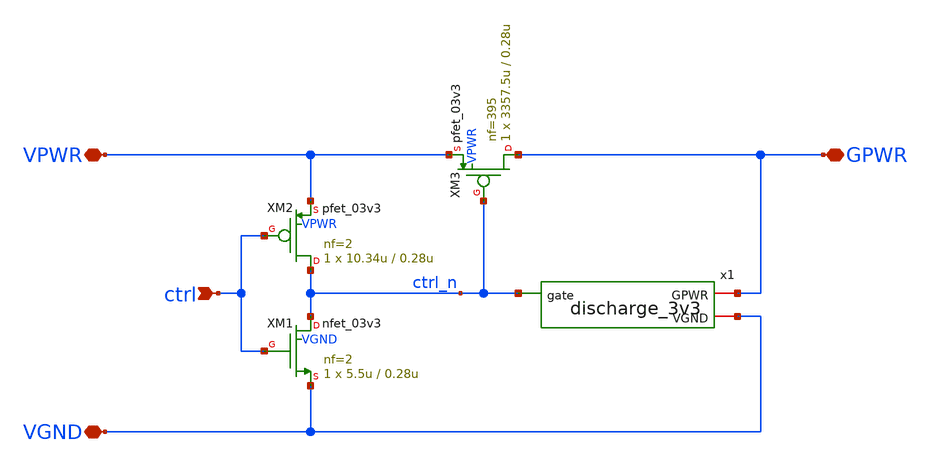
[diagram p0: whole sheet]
** sch_path: pg/gf180mcuD/tt_pg_3v3_hp_2/xschem/tt_pg_3v3_hp_2.sch
**.subckt tt_pg_3v3_hp_2 ctrl VPWR VGND GPWR
*.ipin ctrl
*.iopin VPWR
*.iopin VGND
*.iopin GPWR
x1 VGND GPWR ctrl_n discharge_3v3
XM1 ctrl_n ctrl VGND VGND nfet_03v3 L=0.28u W=5.5u nf=2 ad='int((nf+1)/2) * W/nf * 0.18u' as='int((nf+2)/2) * W/nf * 0.18u'
+ pd='2*int((nf+1)/2) * (W/nf + 0.18u)' ps='2*int((nf+2)/2) * (W/nf + 0.18u)' nrd='0.18u / W' nrs='0.18u / W'
+ sa=0 sb=0 sd=0 m=1 par=1
XM2 ctrl_n ctrl VPWR VPWR pfet_03v3 L=0.28u W=10.34u nf=2 ad='int((nf+1)/2) * W/nf * 0.18u' as='int((nf+2)/2) * W/nf * 0.18u'
+ pd='2*int((nf+1)/2) * (W/nf + 0.18u)' ps='2*int((nf+2)/2) * (W/nf + 0.18u)' nrd='0.18u / W' nrs='0.18u / W'
+ sa=0 sb=0 sd=0 m=1 par=1
XM3 GPWR ctrl_n VPWR VPWR pfet_03v3 L=0.28u W=3357.5u nf=395 ad='int((nf+1)/2) * W/nf * 0.18u' as='int((nf+2)/2) * W/nf * 0.18u'
+ pd='2*int((nf+1)/2) * (W/nf + 0.18u)' ps='2*int((nf+2)/2) * (W/nf + 0.18u)' nrd='0.18u / W' nrs='0.18u / W'
+ sa=0 sb=0 sd=0 m=1 par=1
**.ends

* expanding   symbol:  discharge_3v3.sym # of pins=3
** sym_path: pg/gf180mcuD/common/xschem/discharge_3v3.sym
** sch_path: pg/gf180mcuD/common/xschem/discharge_3v3.sch
.subckt discharge_3v3 VGND GPWR gate
*.iopin GPWR
*.iopin VGND
*.ipin gate
XM1 GPWR gate net3 VGND nfet_03v3 L=0.6u W=0.99u nf=1 ad='int((nf+1)/2) * W/nf * 0.18u' as='int((nf+2)/2) * W/nf * 0.18u'
+ pd='2*int((nf+1)/2) * (W/nf + 0.18u)' ps='2*int((nf+2)/2) * (W/nf + 0.18u)' nrd='0.18u / W' nrs='0.18u / W'
+ sa=0 sb=0 sd=0 m=1 par=1
XM2 net3 gate net2 VGND nfet_03v3 L=0.6u W=0.99u nf=1 ad='int((nf+1)/2) * W/nf * 0.18u' as='int((nf+2)/2) * W/nf * 0.18u'
+ pd='2*int((nf+1)/2) * (W/nf + 0.18u)' ps='2*int((nf+2)/2) * (W/nf + 0.18u)' nrd='0.18u / W' nrs='0.18u / W'
+ sa=0 sb=0 sd=0 m=1 par=1
XM3 net2 gate net1 VGND nfet_03v3 L=0.6u W=0.99u nf=1 ad='int((nf+1)/2) * W/nf * 0.18u' as='int((nf+2)/2) * W/nf * 0.18u'
+ pd='2*int((nf+1)/2) * (W/nf + 0.18u)' ps='2*int((nf+2)/2) * (W/nf + 0.18u)' nrd='0.18u / W' nrs='0.18u / W'
+ sa=0 sb=0 sd=0 m=1 par=1
XM4 net1 gate VGND VGND nfet_03v3 L=0.6u W=0.99u nf=1 ad='int((nf+1)/2) * W/nf * 0.18u' as='int((nf+2)/2) * W/nf * 0.18u'
+ pd='2*int((nf+1)/2) * (W/nf + 0.18u)' ps='2*int((nf+2)/2) * (W/nf + 0.18u)' nrd='0.18u / W' nrs='0.18u / W'
+ sa=0 sb=0 sd=0 m=1 par=1
XM5 GPWR gate net6 VGND nfet_03v3 L=0.6u W=0.99u nf=1 ad='int((nf+1)/2) * W/nf * 0.18u' as='int((nf+2)/2) * W/nf * 0.18u'
+ pd='2*int((nf+1)/2) * (W/nf + 0.18u)' ps='2*int((nf+2)/2) * (W/nf + 0.18u)' nrd='0.18u / W' nrs='0.18u / W'
+ sa=0 sb=0 sd=0 m=1 par=1
XM6 net6 gate net5 VGND nfet_03v3 L=0.6u W=0.99u nf=1 ad='int((nf+1)/2) * W/nf * 0.18u' as='int((nf+2)/2) * W/nf * 0.18u'
+ pd='2*int((nf+1)/2) * (W/nf + 0.18u)' ps='2*int((nf+2)/2) * (W/nf + 0.18u)' nrd='0.18u / W' nrs='0.18u / W'
+ sa=0 sb=0 sd=0 m=1 par=1
XM7 net5 gate net4 VGND nfet_03v3 L=0.6u W=0.99u nf=1 ad='int((nf+1)/2) * W/nf * 0.18u' as='int((nf+2)/2) * W/nf * 0.18u'
+ pd='2*int((nf+1)/2) * (W/nf + 0.18u)' ps='2*int((nf+2)/2) * (W/nf + 0.18u)' nrd='0.18u / W' nrs='0.18u / W'
+ sa=0 sb=0 sd=0 m=1 par=1
XM8 net4 gate VGND VGND nfet_03v3 L=0.6u W=0.99u nf=1 ad='int((nf+1)/2) * W/nf * 0.18u' as='int((nf+2)/2) * W/nf * 0.18u'
+ pd='2*int((nf+1)/2) * (W/nf + 0.18u)' ps='2*int((nf+2)/2) * (W/nf + 0.18u)' nrd='0.18u / W' nrs='0.18u / W'
+ sa=0 sb=0 sd=0 m=1 par=1
.ends

.end
